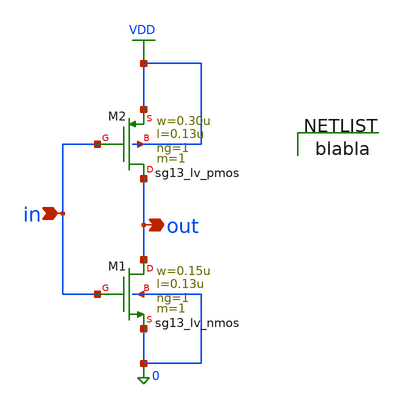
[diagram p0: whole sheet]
** sch_path: 3_real_circuits/inverter.sch
**.subckt inverter in out
*.ipin in
*.opin out
XM1 out in 0 0 sg13_lv_nmos w=0.15u l=0.13u ng=1 m=1 mm_ok=1
XM2 out in VDD VDD sg13_lv_pmos w=0.30u l=0.13u ng=1 m=1 mm_ok=1
**** begin user architecture code

blabla

**** end user architecture code
**.ends
.GLOBAL VDD
.end
